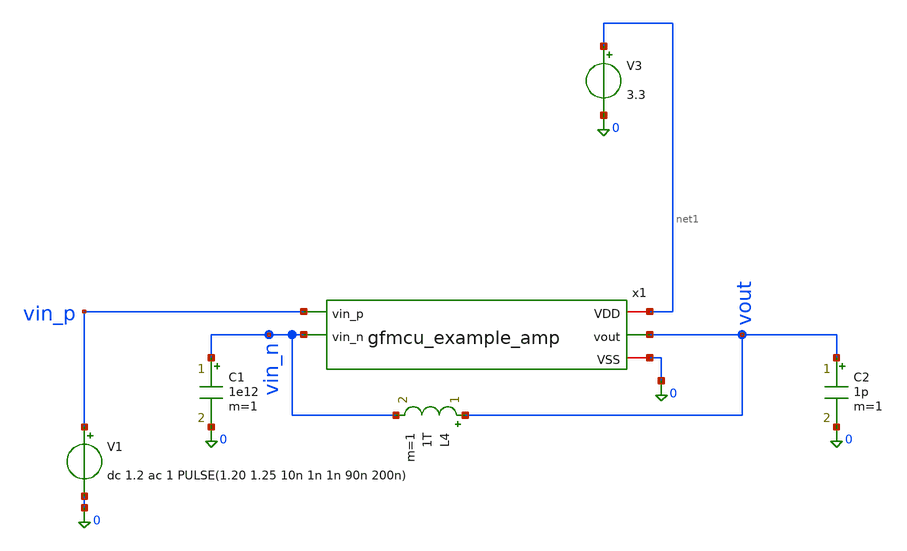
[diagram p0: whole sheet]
** sch_path: xschem/tb_example_amp.sch
**.subckt tb_example_amp
V3 net1 0 3.3
C2 vout 0 1p m=1
V1 vin_p 0 dc 1.2 ac 1 PULSE(1.20 1.25 10n 1n 1n 90n 200n)
L4 vout vin_n 1T m=1
C1 vin_n 0 1e12 m=1
x1 net1 vin_n vin_p vout 0 gfmcu_example_amp
**** begin user architecture code


* GF180MCU Global Process & Noise Parameters (Must be before .lib)
.param fnoicor = 0
.param sw_stat_global = 0
.param sw_stat_mismatch = 10

* PDK Model Include (MOSFETs)
.include /foss/pdks/ciel/gf180mcu/versions/026824c7969ce6f4fc9678e6ca04b0a06a596c4b/gf180mcuD/libs.tech/ngspice/design.ngspice
.lib /foss/pdks/ciel/gf180mcu/versions/026824c7969ce6f4fc9678e6ca04b0a06a596c4b/gf180mcuD/libs.tech/ngspice/sm141064.ngspice typical
.lib /foss/pdks/ciel/gf180mcu/versions/026824c7969ce6f4fc9678e6ca04b0a06a596c4b/gf180mcuD/libs.tech/ngspice/sm141064.ngspice res_typical

* MIM Capacitor Model (bypasses missing OSDI library)
.subckt cap_mim_2f0ff c0 c1 c_width=1e-6 c_length=1e-6
C_mim c0 c1 2.5p
.ends cap_mim_2f0ff

* Remove any .ac or .tran lines outside .control so they don't run prematurely
.save all
.control
destroy all

* ======================================================================
* 1. DC OPERATING POINT & POWER
* ======================================================================
op

let v_inp_dc   = v(vin_p)
let v_inn_dc   = v(vin_n)
let v_out_dc   = v(vout)
let i_vdd_ua   = abs(v3#branch) * 1e6
let p_total_mw = i_vdd_ua * 3.3 / 1e3

echo ======================================================================
echo                    1. DC OPERATING VOLTAGES & POWER
echo ======================================================================
print v_inp_dc v_inn_dc v_out_dc
print i_vdd_ua p_total_mw

* ======================================================================
* 2. AUTOMATED TRANSISTOR SATURATION CHECKER
* ======================================================================
let thr = 0.05

* --- Calculate Margins (abs(VDS) - abs(VDSAT)) ---
let m_xm1  = abs(@m.x1.xm1.m0[vds])  - abs(@m.x1.xm1.m0[vdsat])
let m_xm2  = abs(@m.x1.xm2.m0[vds])  - abs(@m.x1.xm2.m0[vdsat])
let m_xm3  = abs(@m.x1.xm3.m0[vds])  - abs(@m.x1.xm3.m0[vdsat])
let m_xm4  = abs(@m.x1.xm4.m0[vds])  - abs(@m.x1.xm4.m0[vdsat])
let m_xm5  = abs(@m.x1.xm5.m0[vds])  - abs(@m.x1.xm5.m0[vdsat])
let m_xm6  = abs(@m.x1.xm6.m0[vds])  - abs(@m.x1.xm6.m0[vdsat])
let m_xm7  = abs(@m.x1.xm7.m0[vds])  - abs(@m.x1.xm7.m0[vdsat])

let m_xm10 = abs(@m.x1.xm10.m0[vds]) - abs(@m.x1.xm10.m0[vdsat])
let m_xm12 = abs(@m.x1.xm12.m0[vds]) - abs(@m.x1.xm12.m0[vdsat])
let m_xm13 = abs(@m.x1.xm13.m0[vds]) - abs(@m.x1.xm13.m0[vdsat])
let m_xm14 = abs(@m.x1.xm14.m0[vds]) - abs(@m.x1.xm14.m0[vdsat])
let m_xm15 = abs(@m.x1.xm15.m0[vds]) - abs(@m.x1.xm15.m0[vdsat])
let m_xm16 = abs(@m.x1.xm16.m0[vds]) - abs(@m.x1.xm16.m0[vdsat])
let m_xm18 = abs(@m.x1.xm18.m0[vds]) - abs(@m.x1.xm18.m0[vdsat])
let m_xm19 = abs(@m.x1.xm19.m0[vds]) - abs(@m.x1.xm19.m0[vdsat])
let m_xm20 = abs(@m.x1.xm20.m0[vds]) - abs(@m.x1.xm20.m0[vdsat])
let m_xm21 = abs(@m.x1.xm21.m0[vds]) - abs(@m.x1.xm21.m0[vdsat])
let m_xm22 = abs(@m.x1.xm22.m0[vds]) - abs(@m.x1.xm22.m0[vdsat])

echo ======================================================================
echo                  *** TRIODE WARNINGS - MARGIN NEGATIVE ***
echo ======================================================================
if m_xm1 < 0
  echo Bias XM1 PMOS          : $&m_xm1 V
end
if m_xm2 < 0
  echo Bias XM2 PMOS          : $&m_xm2 V
end
if m_xm3 < 0
  echo Bias XM3 PMOS          : $&m_xm3 V
end
if m_xm4 < 0
  echo Bias XM4 NMOS          : $&m_xm4 V
end
if m_xm5 < 0
  echo Bias XM5 NMOS          : $&m_xm5 V
end
if m_xm6 < 0
  echo Bias XM6 NMOS          : $&m_xm6 V
end
if m_xm7 < 0
  echo Bias XM7 NMOS          : $&m_xm7 V
end
if m_xm10 < 0
  echo Amp XM10 PMOS Tail     : $&m_xm10 V
end
if m_xm12 < 0
  echo Amp XM12 PMOS Input L  : $&m_xm12 V
end
if m_xm13 < 0
  echo Amp XM13 PMOS Input R  : $&m_xm13 V
end
if m_xm14 < 0
  echo Amp XM14 PMOS Source L : $&m_xm14 V
end
if m_xm15 < 0
  echo Amp XM15 PMOS Cascode L: $&m_xm15 V
end
if m_xm16 < 0
  echo Amp XM16 PMOS Source R : $&m_xm16 V
end
if m_xm18 < 0
  echo Amp XM18 PMOS Cascode R: $&m_xm18 V
end
if m_xm19 < 0
  echo Amp XM19 NMOS Cascode L: $&m_xm19 V
end
if m_xm20 < 0
  echo Amp XM20 NMOS Load L   : $&m_xm20 V
end
if m_xm21 < 0
  echo Amp XM21 NMOS Cascode R: $&m_xm21 V
end
if m_xm22 < 0
  echo Amp XM22 NMOS Load R   : $&m_xm22 V
end

echo .
echo ======================================================================
echo             *** EDGE OF SATURATION - MARGIN 0 TO 50mV ***
echo ======================================================================
if m_xm1 > 0
  if m_xm1 < thr
    echo Bias XM1 PMOS          : $&m_xm1 V
  end
end
if m_xm2 > 0
  if m_xm2 < thr
    echo Bias XM2 PMOS          : $&m_xm2 V
  end
end
if m_xm3 > 0
  if m_xm3 < thr
    echo Bias XM3 PMOS          : $&m_xm3 V
  end
end
if m_xm4 > 0
  if m_xm4 < thr
    echo Bias XM4 NMOS          : $&m_xm4 V
  end
end
if m_xm5 > 0
  if m_xm5 < thr
    echo Bias XM5 NMOS          : $&m_xm5 V
  end
end
if m_xm6 > 0
  if m_xm6 < thr
    echo Bias XM6 NMOS          : $&m_xm6 V
  end
end
if m_xm7 > 0
  if m_xm7 < thr
    echo Bias XM7 NMOS          : $&m_xm7 V
  end
end
if m_xm10 > 0
  if m_xm10 < thr
    echo Amp XM10 PMOS Tail     : $&m_xm10 V
  end
end
if m_xm12 > 0
  if m_xm12 < thr
    echo Amp XM12 PMOS Input L  : $&m_xm12 V
  end
end
if m_xm13 > 0
  if m_xm13 < thr
    echo Amp XM13 PMOS Input R  : $&m_xm13 V
  end
end
if m_xm14 > 0
  if m_xm14 < thr
    echo Amp XM14 PMOS Source L : $&m_xm14 V
  end
end
if m_xm15 > 0
  if m_xm15 < thr
    echo Amp XM15 PMOS Cascode L: $&m_xm15 V
  end
end
if m_xm16 > 0
  if m_xm16 < thr
    echo Amp XM16 PMOS Source R : $&m_xm16 V
  end
end
if m_xm18 > 0
  if m_xm18 < thr
    echo Amp XM18 PMOS Cascode R: $&m_xm18 V
  end
end
if m_xm19 > 0
  if m_xm19 < thr
    echo Amp XM19 NMOS Cascode L: $&m_xm19 V
  end
end
if m_xm20 > 0
  if m_xm20 < thr
    echo Amp XM20 NMOS Load L   : $&m_xm20 V
  end
end
if m_xm21 > 0
  if m_xm21 < thr
    echo Amp XM21 NMOS Cascode R: $&m_xm21 V
  end
end
if m_xm22 > 0
  if m_xm22 < thr
    echo Amp XM22 NMOS Load R   : $&m_xm22 V
  end
end

* ======================================================================
* 3. AC FREQUENCY RESPONSE (OPEN-LOOP: L4=1e12, C1=1e12)
* ======================================================================
alter l4 = 1e12
alter c1 = 1e12
ac dec 35 1 5G

let v_out_ac  = v(vout)
let gain_db   = db(v_out_ac)
let phase_deg = cph(v_out_ac) * 180 / 3.1415926535

meas ac dc_gain find gain_db at=1
let g_3db = dc_gain - 3
meas ac f_3db when gain_db = g_3db
meas ac f_ugbw when gain_db = 0
meas ac ph_ugbw find phase_deg when gain_db = 0
let pm = 180 + ph_ugbw

echo ======================================================================
echo                    3. AC FREQUENCY RESPONSE RESULTS
echo ======================================================================
print dc_gain
print f_3db
print f_ugbw
print pm

* ======================================================================
* 4. TRANSIENT & SLEW RATE (CLOSED-LOOP UNITY-GAIN: L4=1p, C1=1f)
* ======================================================================
alter l4 = 1e-12
alter c1 = 1e-18
tran 0.1n 1000n

meas tran v_init find v(vout) at=9n
meas tran v_max MAX v(vout) from=10n to=100n
meas tran v_min MIN v(vout) from=100n to=200n

meas tran t_rise TRIG v(vout) VAL=1.21 RISE=1 TARG v(vout) VAL=1.24 RISE=1 from=10n
meas tran t_fall TRIG v(vout) VAL=1.24 FALL=1 TARG v(vout) VAL=1.21 FALL=1 from=50n

let sr_rise_v_us = (0.03 / t_rise) / 1e6
let sr_fall_v_us = (0.03 / t_fall) / 1e6

echo ======================================================================
echo                    4. TRANSIENT & SLEW RATE RESULTS
echo ======================================================================
print v_init v_max v_min
print t_rise sr_rise_v_us
print t_fall sr_fall_v_us

* ======================================================================
* 5. DC SWEEP (OUTPUT SWING & ICMR)
* ======================================================================
alter l4 = 1e-12
alter c1 = 1e-18

* Explicitly save variables so the ICMR curves plot correctly during DC sweep
save all @m.x1.xm10.m0[vds] @m.x1.xm10.m0[vdsat] @m.x1.xm12.m0[vds] @m.x1.xm12.m0[vdsat]
dc v1 0 3.3 1m

let vout_deriv = deriv(v(vout))
meas dc swing_min find v(vout) when vout_deriv=0.9 cross=1
meas dc swing_max find v(vout) when vout_deriv=0.9 cross=last
let total_swing = swing_max - swing_min

* Calculate ICMR Margins for the PMOS Tail and PMOS Input Pair
let m_tail_sweep = abs(@m.x1.xm10.m0[vds]) - abs(@m.x1.xm10.m0[vdsat])
let m_in_sweep   = abs(@m.x1.xm12.m0[vds]) - abs(@m.x1.xm12.m0[vdsat])

echo ======================================================================
echo                    5. OUTPUT SWING RESULTS
echo ======================================================================
print swing_min swing_max total_swing

* ======================================================================
* 6. NOISE ANALYSIS
* ======================================================================
* Reset save behavior so noise spectrum saves correctly
save all
noise v(vout) v1 dec 35 1 5G

echo ======================================================================
echo                    6. NOISE ANALYSIS RESULTS
echo ======================================================================
print inoise_total onoise_total

* ======================================================================
* 7. PLOTS
* ======================================================================
setplot ac1
plot db(v(vout)) title 'Open-Loop Gain (dB)'
plot (cph(v(vout))*180/3.14159265) title 'Open-Loop Phase (Deg)'

setplot tran1
plot v(vout) v(vin_p) title 'Closed-Loop Transient Step Response'

setplot dc1
plot v(vout) v(vin_p) title 'DC Transfer Characteristic (Output Swing)'
*plot m_tail_sweep m_in_sweep title 'ICMR: Saturation Margins (>0 is good)'

*setplot noise1
*plot inoise_spectrum title 'Input-Referred Noise Spectrum (V/rtHz)'

.endc


**** end user architecture code
**.ends

* expanding   symbol:  ttgf-ece298-analog-op-amp/xschem/gfmcu_example_amp.sym # of pins=5
** sym_path: xschem/gfmcu_example_amp.sym
** sch_path: xschem/gfmcu_example_amp.sch
.subckt gfmcu_example_amp VDD vin_n vin_p vout VSS
*.ipin vin_n
*.ipin vin_p
*.opin vout
*.iopin VSS
*.iopin VDD
XM1 net6 net2 net1 VDD pfet_03v3 L=0.84u W=4u nf=4 ad='int((nf+1)/2) * W/nf * 0.18u' as='int((nf+2)/2)
+ * W/nf * 0.18u' pd='2*int((nf+1)/2) * (W/nf + 0.18u)' ps='2*int((nf+2)/2) * (W/nf + 0.18u)' nrd='0.18u
+ / W' nrs='0.18u / W' sa=0 sb=0 sd=0 m=2 par=2
XM2 net3 net3 VDD VDD pfet_03v3 L=0.28u W=4u nf=4 ad='int((nf+1)/2) * W/nf * 0.18u' as='int((nf+2)/2)
+ * W/nf * 0.18u' pd='2*int((nf+1)/2) * (W/nf + 0.18u)' ps='2*int((nf+2)/2) * (W/nf + 0.18u)' nrd='0.18u
+ / W' nrs='0.18u / W' sa=0 sb=0 sd=0 m=2 par=2
XM3 net2 net2 net3 VDD pfet_03v3 L=0.84u W=4u nf=4 ad='int((nf+1)/2) * W/nf * 0.18u' as='int((nf+2)/2)
+ * W/nf * 0.18u' pd='2*int((nf+1)/2) * (W/nf + 0.18u)' ps='2*int((nf+2)/2) * (W/nf + 0.18u)' nrd='0.18u
+ / W' nrs='0.18u / W' sa=0 sb=0 sd=0 m=2 par=2
XM4 net6 net6 net5 VSS nfet_03v3 L=0.84u W=4u nf=4 ad='int((nf+1)/2) * W/nf * 0.18u' as='int((nf+2)/2)
+ * W/nf * 0.18u' pd='2*int((nf+1)/2) * (W/nf + 0.18u)' ps='2*int((nf+2)/2) * (W/nf + 0.18u)' nrd='0.18u
+ / W' nrs='0.18u / W' sa=0 sb=0 sd=0 m=2 par=2
XM5 net5 net5 VSS VSS nfet_03v3 L=0.84u W=4u nf=4 ad='int((nf+1)/2) * W/nf * 0.18u' as='int((nf+2)/2)
+ * W/nf * 0.18u' pd='2*int((nf+1)/2) * (W/nf + 0.18u)' ps='2*int((nf+2)/2) * (W/nf + 0.18u)' nrd='0.18u
+ / W' nrs='0.18u / W' sa=0 sb=0 sd=0 m=2 par=2
XM6 net2 net6 net4 VSS nfet_03v3 L=0.84u W=4u nf=4 ad='int((nf+1)/2) * W/nf * 0.18u' as='int((nf+2)/2)
+ * W/nf * 0.18u' pd='2*int((nf+1)/2) * (W/nf + 0.18u)' ps='2*int((nf+2)/2) * (W/nf + 0.18u)' nrd='0.18u
+ / W' nrs='0.18u / W' sa=0 sb=0 sd=0 m=2 par=2
XM7 net4 net5 VSS VSS nfet_03v3 L=0.84u W=4u nf=4 ad='int((nf+1)/2) * W/nf * 0.18u' as='int((nf+2)/2)
+ * W/nf * 0.18u' pd='2*int((nf+1)/2) * (W/nf + 0.18u)' ps='2*int((nf+2)/2) * (W/nf + 0.18u)' nrd='0.18u
+ / W' nrs='0.18u / W' sa=0 sb=0 sd=0 m=2 par=2
XM10 net7 net8 VDD VDD pfet_03v3 L=0.84u W=4u nf=4 ad='int((nf+1)/2) * W/nf * 0.18u' as='int((nf+2)/2)
+ * W/nf * 0.18u' pd='2*int((nf+1)/2) * (W/nf + 0.18u)' ps='2*int((nf+2)/2) * (W/nf + 0.18u)' nrd='0.18u
+ / W' nrs='0.18u / W' sa=0 sb=0 sd=0 m=2 par=2
XM12 net10 vin_p net7 VDD pfet_03v3 L=0.84u W=4u nf=4 ad='int((nf+1)/2) * W/nf * 0.18u' as='int((nf+2)/2)
+ * W/nf * 0.18u' pd='2*int((nf+1)/2) * (W/nf + 0.18u)' ps='2*int((nf+2)/2) * (W/nf + 0.18u)' nrd='0.18u
+ / W' nrs='0.18u / W' sa=0 sb=0 sd=0 m=16 par=16
XM13 net9 vin_n net7 VDD pfet_03v3 L=0.84u W=4u nf=4 ad='int((nf+1)/2) * W/nf * 0.18u' as='int((nf+2)/2)
+ * W/nf * 0.18u' pd='2*int((nf+1)/2) * (W/nf + 0.18u)' ps='2*int((nf+2)/2) * (W/nf + 0.18u)' nrd='0.18u
+ / W' nrs='0.18u / W' sa=0 sb=0 sd=0 m=16 par=16
XM14 net11 net8 VDD VDD pfet_03v3 L=0.84u W=4u nf=4 ad='int((nf+1)/2) * W/nf * 0.18u' as='int((nf+2)/2)
+ * W/nf * 0.18u' pd='2*int((nf+1)/2) * (W/nf + 0.18u)' ps='2*int((nf+2)/2) * (W/nf + 0.18u)' nrd='0.18u
+ / W' nrs='0.18u / W' sa=0 sb=0 sd=0 m=2 par=2
XM15 net8 net12 net11 VDD pfet_03v3 L=0.84u W=4u nf=4 ad='int((nf+1)/2) * W/nf * 0.18u' as='int((nf+2)/2)
+ * W/nf * 0.18u' pd='2*int((nf+1)/2) * (W/nf + 0.18u)' ps='2*int((nf+2)/2) * (W/nf + 0.18u)' nrd='0.18u
+ / W' nrs='0.18u / W' sa=0 sb=0 sd=0 m=2 par=2
XR2 net12 net8 VDD ppolyf_u r_width=0.5 r_length=20 m=1
XM16 net13 net8 VDD VDD pfet_03v3 L=0.84u W=4u nf=4 ad='int((nf+1)/2) * W/nf * 0.18u' as='int((nf+2)/2)
+ * W/nf * 0.18u' pd='2*int((nf+1)/2) * (W/nf + 0.18u)' ps='2*int((nf+2)/2) * (W/nf + 0.18u)' nrd='0.18u
+ / W' nrs='0.18u / W' sa=0 sb=0 sd=0 m=2 par=2
XM18 vout net12 net13 VDD pfet_03v3 L=0.84u W=4u nf=4 ad='int((nf+1)/2) * W/nf * 0.18u' as='int((nf+2)/2)
+ * W/nf * 0.18u' pd='2*int((nf+1)/2) * (W/nf + 0.18u)' ps='2*int((nf+2)/2) * (W/nf + 0.18u)' nrd='0.18u
+ / W' nrs='0.18u / W' sa=0 sb=0 sd=0 m=2 par=2
XM19 net12 net6 net10 VSS nfet_03v3 L=0.84u W=4u nf=4 ad='int((nf+1)/2) * W/nf * 0.18u' as='int((nf+2)/2)
+ * W/nf * 0.18u' pd='2*int((nf+1)/2) * (W/nf + 0.18u)' ps='2*int((nf+2)/2) * (W/nf + 0.18u)' nrd='0.18u
+ / W' nrs='0.18u / W' sa=0 sb=0 sd=0 m=2 par=2
XM20 net10 net5 VSS VSS nfet_03v3 L=0.84u W=4u nf=4 ad='int((nf+1)/2) * W/nf * 0.18u' as='int((nf+2)/2)
+ * W/nf * 0.18u' pd='2*int((nf+1)/2) * (W/nf + 0.18u)' ps='2*int((nf+2)/2) * (W/nf + 0.18u)' nrd='0.18u
+ / W' nrs='0.18u / W' sa=0 sb=0 sd=0 m=2 par=2
XM21 vout net6 net9 VSS nfet_03v3 L=0.84u W=4u nf=4 ad='int((nf+1)/2) * W/nf * 0.18u' as='int((nf+2)/2)
+ * W/nf * 0.18u' pd='2*int((nf+1)/2) * (W/nf + 0.18u)' ps='2*int((nf+2)/2) * (W/nf + 0.18u)' nrd='0.18u
+ / W' nrs='0.18u / W' sa=0 sb=0 sd=0 m=2 par=2
XM22 net9 net5 VSS VSS nfet_03v3 L=0.84u W=4u nf=4 ad='int((nf+1)/2) * W/nf * 0.18u' as='int((nf+2)/2)
+ * W/nf * 0.18u' pd='2*int((nf+1)/2) * (W/nf + 0.18u)' ps='2*int((nf+2)/2) * (W/nf + 0.18u)' nrd='0.18u
+ / W' nrs='0.18u / W' sa=0 sb=0 sd=0 m=2 par=2
I0 VDD net1 2.5e-05
.ends

.end
